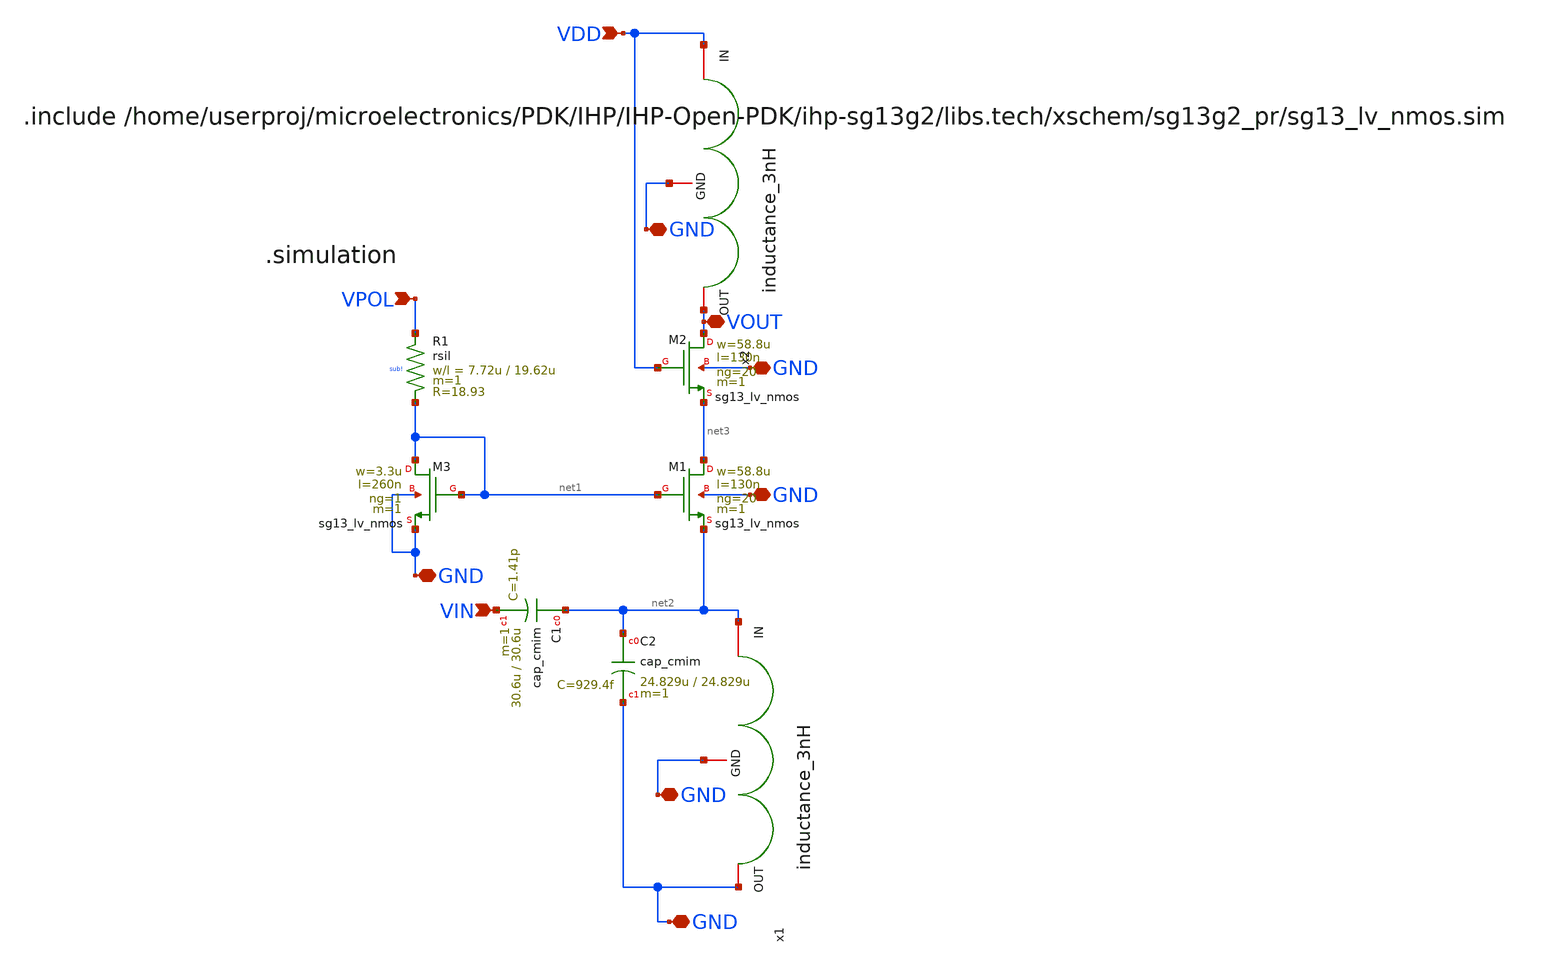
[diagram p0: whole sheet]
** sch_path: LVS/xschem/BGM_AA/LNA_GC_SINGLE/TOP.sch
**.subckt TOP VIN GND VDD VPOL GND GND GND GND GND VOUT
*.ipin VIN
*.iopin GND
*.ipin VDD
*.ipin VPOL
*.iopin GND
*.iopin GND
*.iopin GND
*.iopin GND
*.iopin GND
*.iopin VOUT
XM1 net3 net1 net2 GND sg13_lv_nmos w=58.8u l=130n ng=20 m=1 mm_ok=1
XR1 VPOL net1 sub! rsil w=7.72u l=19.62u m=1 mm_ok=1
XM3 net1 net1 GND GND sg13_lv_nmos w=3.3u l=260n ng=1 m=1 mm_ok=1
XM2 VOUT VDD net3 GND sg13_lv_nmos w=58.8u l=130n ng=20 m=1 mm_ok=1
XC1 net2 VIN cap_cmim w=30.6u l=30.6u m=1 mm_ok=1
XC2 net2 GND cap_cmim w=24.829u l=24.829u m=1 mm_ok=1
x1 GND net2 GND inductance_3nH
x2 VOUT VDD GND inductance_3nH
**.ends

* expanding   symbol:
*+  /home/userproj/microelectronics/projects/ZigBee/Inductance/MODEL_XSCHEM/inductance_3nH.sym # of pins=3
** sym_path: Inductance/MODEL_XSCHEM/inductance_3nH.sym
** sch_path: Inductance/MODEL_XSCHEM/inductance_3nH.sch
.subckt inductance_3nH OUT IN GND
*.iopin GND
*.iopin OUT
*.iopin IN
Ls net1 OUT 2.885n m=1
Cox1 IN net2 55.8f m=1
Cox2 OUT net3 55.8f m=1
Csp IN OUT 13.69f m=1
Rp1 net2 GND 18.32 m=1
Rp2 net3 GND 18.32 m=1
Rs IN net1 3.623 m=1
.ends

.end
